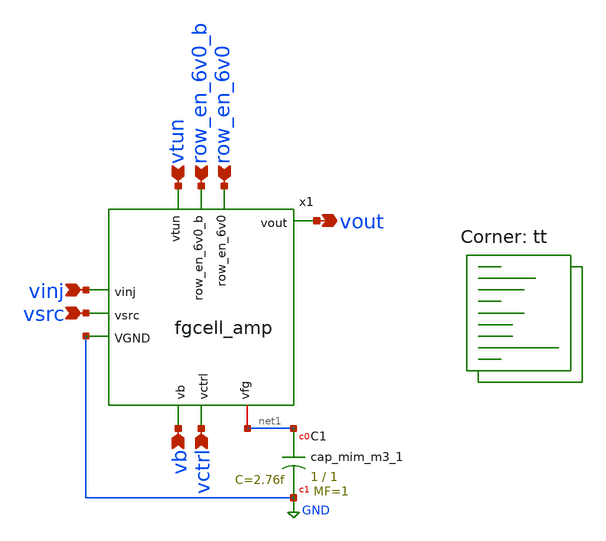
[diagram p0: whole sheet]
** sch_path: xschem/fgcell_amp_MiM_cap_1_1.sch
**.subckt fgcell_amp_MiM_cap_1_1 vinj vsrc vb vctrl vtun row_en_6v0_b row_en_6v0 vout
*.ipin vinj
*.ipin vsrc
*.ipin vb
*.ipin vctrl
*.ipin vtun
*.ipin row_en_6v0_b
*.ipin row_en_6v0
*.opin vout
x1 net1 vctrl vinj row_en_6v0_b vsrc vtun GND vout row_en_6v0 vb fgcell_amp
XC1 net1 GND sky130_fd_pr__cap_mim_m3_1 W=1 L=1 MF=1 m=1
**** begin user architecture code
.lib $::SKYWATER_MODELS/sky130.lib.spice tt
**** end user architecture code
**.ends

* expanding   symbol:  fgcell_amp.sym # of pins=10
** sym_path: xschem/fgcell_amp.sym
** sch_path: xschem/fgcell_amp.sch
.subckt fgcell_amp vfg vctrl vinj row_en_6v0_b vsrc vtun VGND vout row_en_6v0 vb
*.ipin vinj
*.ipin row_en_6v0_b
*.ipin vtun
*.ipin vctrl
*.ipin vsrc
*.ipin vb
*.ipin VGND
*.opin vout
*.iopin vfg
*.ipin row_en_6v0
x1 vinj row_en_6v0_b vtun vctrl vsrc VGND vfg fgcell
x2 vfg net1 VGND vinj vb net1 diffamp_nmos
x3 net1 vout row_en_6v0 row_en_6v0_b vinj VGND tg5v0
.ends


* expanding   symbol:  fgcell.sym # of pins=7
** sym_path: xschem/fgcell.sym
** sch_path: xschem/fgcell.sch
.subckt fgcell vinj vinj_en_b vtun vctrl vsrc VGND vfg
*.ipin vinj
*.ipin vinj_en_b
*.ipin vtun
*.ipin vctrl
*.ipin vsrc
*.ipin VGND
*.opin vfg
XM1 vsrc vfg net1 vinj sky130_fd_pr__pfet_g5v0d10v5 L=0.5 W=1 nf=1 ad='int((nf+1)/2) * W/nf * 0.29' as='int((nf+2)/2) * W/nf * 0.29'
+ pd='2*int((nf+1)/2) * (W/nf + 0.29)' ps='2*int((nf+2)/2) * (W/nf + 0.29)' nrd='0.29 / W' nrs='0.29 / W'
+ sa=0 sb=0 sd=0 mult=1 m=1
XM2 net1 vinj_en_b vinj vinj sky130_fd_pr__pfet_g5v0d10v5 L=0.5 W=1 nf=1 ad='int((nf+1)/2) * W/nf * 0.29'
+ as='int((nf+2)/2) * W/nf * 0.29' pd='2*int((nf+1)/2) * (W/nf + 0.29)' ps='2*int((nf+2)/2) * (W/nf + 0.29)'
+ nrd='0.29 / W' nrs='0.29 / W' sa=0 sb=0 sd=0 mult=1 m=1
XC1 vfg vtun VGND sky130_fd_pr__cap_var_hvt W=1 L=0.5 VM=1 m=1
XM3 vctrl vfg vctrl vctrl sky130_fd_pr__pfet_g5v0d10v5 L=0.5 W=1 nf=1 ad='int((nf+1)/2) * W/nf * 0.29'
+ as='int((nf+2)/2) * W/nf * 0.29' pd='2*int((nf+1)/2) * (W/nf + 0.29)' ps='2*int((nf+2)/2) * (W/nf + 0.29)'
+ nrd='0.29 / W' nrs='0.29 / W' sa=0 sb=0 sd=0 mult=1 m=1
.ends


* expanding   symbol:  diffamp_nmos.sym # of pins=6
** sym_path: xschem/diffamp_nmos.sym
** sch_path: xschem/diffamp_nmos.sch
.subckt diffamp_nmos v1 v2 VSS VDD vb vout
*.ipin v1
*.ipin v2
*.ipin vb
*.opin vout
*.ipin VDD
*.ipin VSS
XM7 int2 int3 VDD VDD sky130_fd_pr__pfet_g5v0d10v5 L=1 W=1.5 nf=1 ad='int((nf+1)/2) * W/nf * 0.29' as='int((nf+2)/2) * W/nf * 0.29'
+ pd='2*int((nf+1)/2) * (W/nf + 0.29)' ps='2*int((nf+2)/2) * (W/nf + 0.29)' nrd='0.29 / W' nrs='0.29 / W'
+ sa=0 sb=0 sd=0 mult=1 m=1
XM8 int2 int2 VSS VSS sky130_fd_pr__nfet_g5v0d10v5 L=1 W=1.5 nf=1 ad='int((nf+1)/2) * W/nf * 0.29' as='int((nf+2)/2) * W/nf * 0.29'
+ pd='2*int((nf+1)/2) * (W/nf + 0.29)' ps='2*int((nf+2)/2) * (W/nf + 0.29)' nrd='0.29 / W' nrs='0.29 / W'
+ sa=0 sb=0 sd=0 mult=1 m=1
XM9 vout int2 VSS VSS sky130_fd_pr__nfet_g5v0d10v5 L=1 W=1.5 nf=1 ad='int((nf+1)/2) * W/nf * 0.29' as='int((nf+2)/2) * W/nf * 0.29'
+ pd='2*int((nf+1)/2) * (W/nf + 0.29)' ps='2*int((nf+2)/2) * (W/nf + 0.29)' nrd='0.29 / W' nrs='0.29 / W'
+ sa=0 sb=0 sd=0 mult=1 m=1
XM1 int4 v1 int1 VSS sky130_fd_pr__nfet_g5v0d10v5 L=1 W=1.5 nf=1 ad='int((nf+1)/2) * W/nf * 0.29' as='int((nf+2)/2) * W/nf * 0.29'
+ pd='2*int((nf+1)/2) * (W/nf + 0.29)' ps='2*int((nf+2)/2) * (W/nf + 0.29)' nrd='0.29 / W' nrs='0.29 / W'
+ sa=0 sb=0 sd=0 mult=1 m=1
XM2 int3 v2 int1 VSS sky130_fd_pr__nfet_g5v0d10v5 L=1 W=1.5 nf=1 ad='int((nf+1)/2) * W/nf * 0.29' as='int((nf+2)/2) * W/nf * 0.29'
+ pd='2*int((nf+1)/2) * (W/nf + 0.29)' ps='2*int((nf+2)/2) * (W/nf + 0.29)' nrd='0.29 / W' nrs='0.29 / W'
+ sa=0 sb=0 sd=0 mult=1 m=1
XM6 int3 int3 VDD VDD sky130_fd_pr__pfet_g5v0d10v5 L=1 W=1.5 nf=1 ad='int((nf+1)/2) * W/nf * 0.29' as='int((nf+2)/2) * W/nf * 0.29'
+ pd='2*int((nf+1)/2) * (W/nf + 0.29)' ps='2*int((nf+2)/2) * (W/nf + 0.29)' nrd='0.29 / W' nrs='0.29 / W'
+ sa=0 sb=0 sd=0 mult=1 m=1
XM5 vout int4 VDD VDD sky130_fd_pr__pfet_g5v0d10v5 L=1 W=1.5 nf=1 ad='int((nf+1)/2) * W/nf * 0.29' as='int((nf+2)/2) * W/nf * 0.29'
+ pd='2*int((nf+1)/2) * (W/nf + 0.29)' ps='2*int((nf+2)/2) * (W/nf + 0.29)' nrd='0.29 / W' nrs='0.29 / W'
+ sa=0 sb=0 sd=0 mult=1 m=1
XM3a int1 vb int5 VSS sky130_fd_pr__nfet_g5v0d10v5 L=1 W=1.5 nf=1 ad='int((nf+1)/2) * W/nf * 0.29' as='int((nf+2)/2) * W/nf * 0.29'
+ pd='2*int((nf+1)/2) * (W/nf + 0.29)' ps='2*int((nf+2)/2) * (W/nf + 0.29)' nrd='0.29 / W' nrs='0.29 / W'
+ sa=0 sb=0 sd=0 mult=1 m=1
XM3b int5 vb VSS VSS sky130_fd_pr__nfet_g5v0d10v5 L=1 W=1.5 nf=1 ad='int((nf+1)/2) * W/nf * 0.29' as='int((nf+2)/2) * W/nf * 0.29'
+ pd='2*int((nf+1)/2) * (W/nf + 0.29)' ps='2*int((nf+2)/2) * (W/nf + 0.29)' nrd='0.29 / W' nrs='0.29 / W'
+ sa=0 sb=0 sd=0 mult=1 m=1
XM4 int4 int4 VDD VDD sky130_fd_pr__pfet_g5v0d10v5 L=1 W=1.5 nf=1 ad='int((nf+1)/2) * W/nf * 0.29' as='int((nf+2)/2) * W/nf * 0.29'
+ pd='2*int((nf+1)/2) * (W/nf + 0.29)' ps='2*int((nf+2)/2) * (W/nf + 0.29)' nrd='0.29 / W' nrs='0.29 / W'
+ sa=0 sb=0 sd=0 mult=1 m=1
.ends


* expanding   symbol:  tg5v0.sym # of pins=6
** sym_path: xschem/tg5v0.sym
** sch_path: xschem/tg5v0.sch
.subckt tg5v0 vin vout en en_b vdd vss
*.ipin vin
*.opin vout
*.ipin en
*.ipin en_b
*.ipin vdd
*.ipin vss
XM1 vout en vin vss sky130_fd_pr__nfet_g5v0d10v5 L=0.5 W=4 nf=8 ad='int((nf+1)/2) * W/nf * 0.29' as='int((nf+2)/2) * W/nf * 0.29'
+ pd='2*int((nf+1)/2) * (W/nf + 0.29)' ps='2*int((nf+2)/2) * (W/nf + 0.29)' nrd='0.29 / W' nrs='0.29 / W'
+ sa=0 sb=0 sd=0 mult=1 m=1
XM2 vout en_b vin vdd sky130_fd_pr__pfet_g5v0d10v5 L=0.5 W=4 nf=8 ad='int((nf+1)/2) * W/nf * 0.29' as='int((nf+2)/2) * W/nf * 0.29'
+ pd='2*int((nf+1)/2) * (W/nf + 0.29)' ps='2*int((nf+2)/2) * (W/nf + 0.29)' nrd='0.29 / W' nrs='0.29 / W'
+ sa=0 sb=0 sd=0 mult=1 m=1
.ends

.GLOBAL GND
.end
